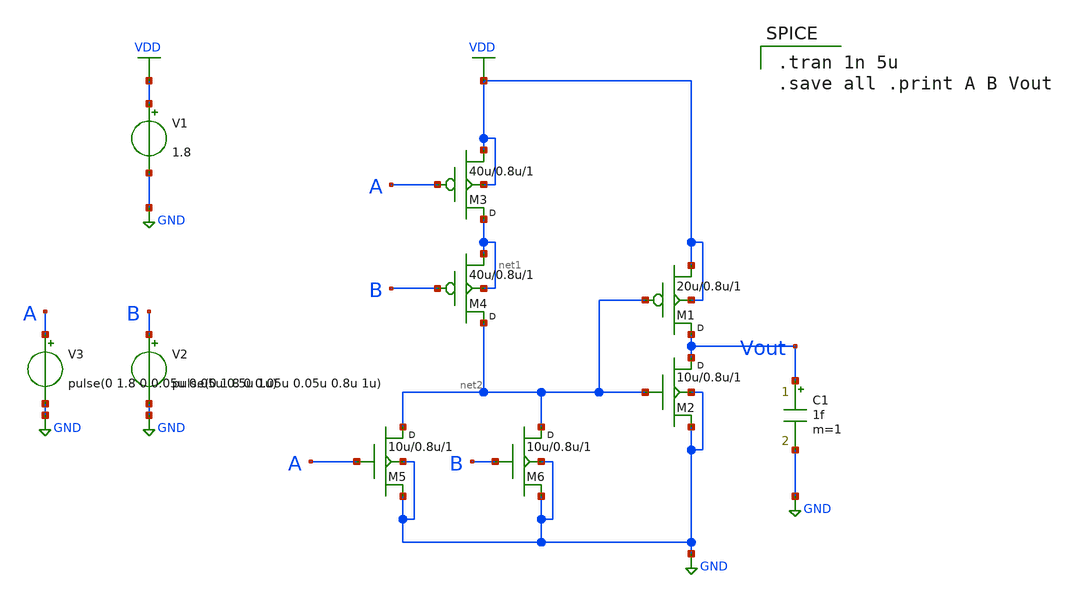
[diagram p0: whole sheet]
** sch_path: cells/or2/or-gate.sch
**.subckt or-gate
M1 Vout net2 VDD VDD pmos w=20u l=0.8u m=1
M2 Vout net2 GND GND nmos w=10u l=0.8u m=1
V1 VDD GND 1.8
M3 net1 A VDD VDD pmos w=40u l=0.8u m=1
M4 net2 B net1 net1 pmos w=40u l=0.8u m=1
M5 net2 A GND GND nmos w=10u l=0.8u m=1
M6 net2 B GND GND nmos w=10u l=0.8u m=1
V2 B GND pulse(0 1.8 0 0.05u 0.05u 0.8u 1u)
V3 A GND pulse(0 1.8 0 0.05u 0.05u 0.5u 1u)
C1 Vout GND 1f m=1
**** begin user architecture code

.tran 1n 5u
.save all .print A B Vout



.model nmos nmos level=49 version=3.3.0
.model pmos pmos level=49 version=3.3.0

**** end user architecture code
**.ends
.GLOBAL GND
.GLOBAL VDD
.end
